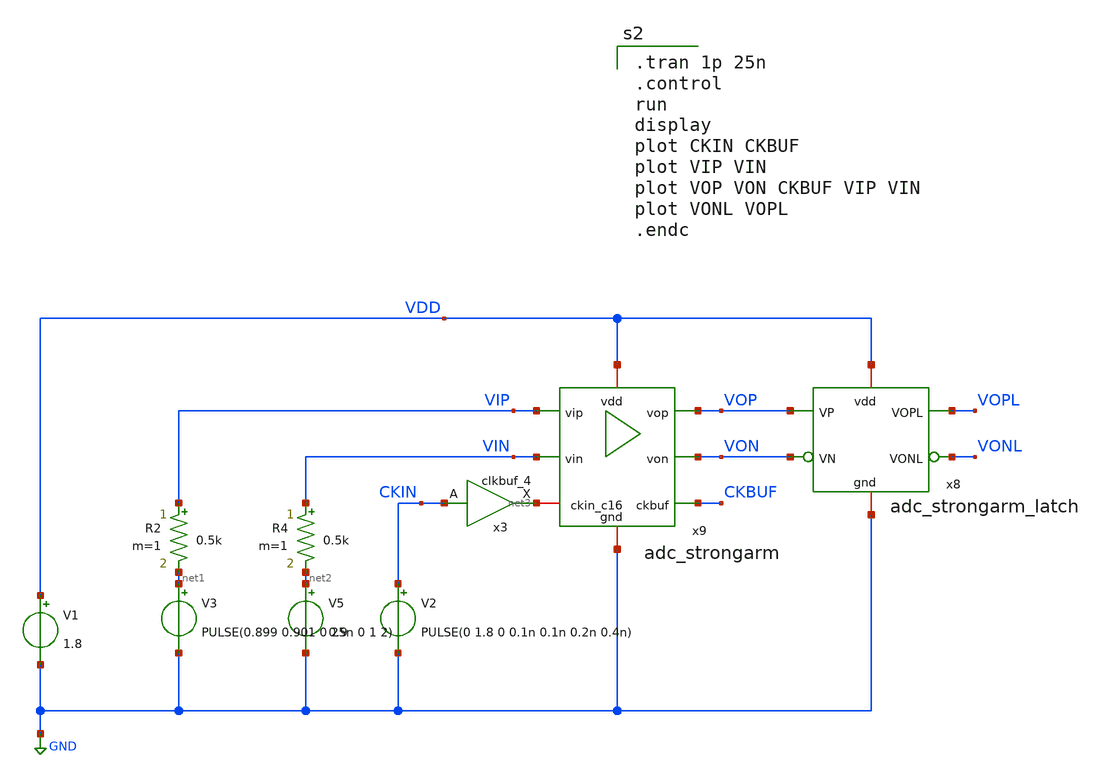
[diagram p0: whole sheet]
** sch_path: xschem/adc_strongarm_tb.sch
**.subckt adc_strongarm_tb
V1 VDD GND 1.8
V2 CKIN GND PULSE(0 1.8 0 0.1n 0.1n 0.2n 0.4n)
V3 net1 GND PULSE(0.899 0.901 0 25n 0 1 2)
x3 CKIN GND GND VDD VDD net3 sky130_fd_sc_hs__clkbuf_4
R2 VIP net1 0.5k m=1
x8 VONL VOPL VDD GND VOP VON adc_strongarm_latch
x9 VDD VOP VON VIP VIN net3 GND CKBUF adc_strongarm
V5 net2 GND 0.9
R4 VIN net2 0.5k m=1
**** begin user architecture code

.tran 1p 25n
.control
run
display
plot CKIN CKBUF
plot VIP VIN
plot VOP VON CKBUF VIP VIN
plot VONL VOPL
.endc


.lib $::SKYWATER_MODELS/sky130.lib.spice tt
.include $::PDKPATH/libs.ref/sky130_fd_sc_hs/spice/sky130_fd_sc_hs.spice

**** end user architecture code
**.ends

* expanding   symbol:  adc_strongarm_latch.sym # of pins=6
** sym_path: xschem/adc_strongarm_latch.sym
** sch_path: xschem/adc_strongarm_latch.sch
.subckt adc_strongarm_latch VONL VOPL vdd gnd VP VN
*.iopin vdd
*.iopin gnd
*.ipin VP
*.ipin VN
*.opin VOPL
*.opin VONL
XM11 VOPL net1 gnd gnd sky130_fd_pr__nfet_01v8 L=0.15 W=5 nf=1 ad='int((nf+1)/2) * W/nf * 0.29' as='int((nf+2)/2) * W/nf * 0.29'
+ pd='2*int((nf+1)/2) * (W/nf + 0.29)' ps='2*int((nf+2)/2) * (W/nf + 0.29)' nrd='0.29 / W' nrs='0.29 / W'
+ sa=0 sb=0 sd=0 mult=1 m=1
XM12 VONL net2 gnd gnd sky130_fd_pr__nfet_01v8 L=0.15 W=5 nf=1 ad='int((nf+1)/2) * W/nf * 0.29' as='int((nf+2)/2) * W/nf * 0.29'
+ pd='2*int((nf+1)/2) * (W/nf + 0.29)' ps='2*int((nf+2)/2) * (W/nf + 0.29)' nrd='0.29 / W' nrs='0.29 / W'
+ sa=0 sb=0 sd=0 mult=1 m=1
x6 VOPL gnd gnd vdd vdd VONL sky130_fd_sc_hd__inv_1
x7 VONL gnd gnd vdd vdd VOPL sky130_fd_sc_hd__inv_1
x1 VP gnd gnd vdd vdd net1 sky130_fd_sc_hd__inv_1
x2 VN gnd gnd vdd vdd net2 sky130_fd_sc_hd__inv_1
.ends


* expanding   symbol:  adc_strongarm.sym # of pins=8
** sym_path: xschem/adc_strongarm.sym
** sch_path: xschem/adc_strongarm.sch
.subckt adc_strongarm vdd vop von vip vin ckin_c16 gnd ckbuf
*.ipin vip
*.ipin vin
*.iopin gnd
*.iopin vdd
*.opin vop
*.opin von
*.iopin ckin_c16
*.opin ckbuf
XM1 net3 vip net1 gnd sky130_fd_pr__nfet_01v8 L=0.15 W=10 nf=1 ad='int((nf+1)/2) * W/nf * 0.29' as='int((nf+2)/2) * W/nf * 0.29'
+ pd='2*int((nf+1)/2) * (W/nf + 0.29)' ps='2*int((nf+2)/2) * (W/nf + 0.29)' nrd='0.29 / W' nrs='0.29 / W'
+ sa=0 sb=0 sd=0 mult=2 m=2
XM2 net2 vin net1 gnd sky130_fd_pr__nfet_01v8 L=0.15 W=10 nf=1 ad='int((nf+1)/2) * W/nf * 0.29' as='int((nf+2)/2) * W/nf * 0.29'
+ pd='2*int((nf+1)/2) * (W/nf + 0.29)' ps='2*int((nf+2)/2) * (W/nf + 0.29)' nrd='0.29 / W' nrs='0.29 / W'
+ sa=0 sb=0 sd=0 mult=2 m=2
XM3 net1 ckbuf gnd gnd sky130_fd_pr__nfet_01v8 L=0.15 W=20 nf=1 ad='int((nf+1)/2) * W/nf * 0.29' as='int((nf+2)/2) * W/nf * 0.29'
+ pd='2*int((nf+1)/2) * (W/nf + 0.29)' ps='2*int((nf+2)/2) * (W/nf + 0.29)' nrd='0.29 / W' nrs='0.29 / W'
+ sa=0 sb=0 sd=0 mult=2 m=2
XM4 vop von net3 gnd sky130_fd_pr__nfet_01v8 L=0.15 W=10 nf=1 ad='int((nf+1)/2) * W/nf * 0.29' as='int((nf+2)/2) * W/nf * 0.29'
+ pd='2*int((nf+1)/2) * (W/nf + 0.29)' ps='2*int((nf+2)/2) * (W/nf + 0.29)' nrd='0.29 / W' nrs='0.29 / W'
+ sa=0 sb=0 sd=0 mult=2 m=2
XM5 von vop net2 gnd sky130_fd_pr__nfet_01v8 L=0.15 W=10 nf=1 ad='int((nf+1)/2) * W/nf * 0.29' as='int((nf+2)/2) * W/nf * 0.29'
+ pd='2*int((nf+1)/2) * (W/nf + 0.29)' ps='2*int((nf+2)/2) * (W/nf + 0.29)' nrd='0.29 / W' nrs='0.29 / W'
+ sa=0 sb=0 sd=0 mult=2 m=2
XM6 von vop vdd vdd sky130_fd_pr__pfet_01v8 L=0.15 W=20 nf=1 ad='int((nf+1)/2) * W/nf * 0.29' as='int((nf+2)/2) * W/nf * 0.29'
+ pd='2*int((nf+1)/2) * (W/nf + 0.29)' ps='2*int((nf+2)/2) * (W/nf + 0.29)' nrd='0.29 / W' nrs='0.29 / W'
+ sa=0 sb=0 sd=0 mult=2 m=2
XM7 vop von vdd vdd sky130_fd_pr__pfet_01v8 L=0.15 W=20 nf=1 ad='int((nf+1)/2) * W/nf * 0.29' as='int((nf+2)/2) * W/nf * 0.29'
+ pd='2*int((nf+1)/2) * (W/nf + 0.29)' ps='2*int((nf+2)/2) * (W/nf + 0.29)' nrd='0.29 / W' nrs='0.29 / W'
+ sa=0 sb=0 sd=0 mult=2 m=2
XM8 vop ckbuf vdd vdd sky130_fd_pr__pfet_01v8 L=0.15 W=10 nf=1 ad='int((nf+1)/2) * W/nf * 0.29' as='int((nf+2)/2) * W/nf * 0.29'
+ pd='2*int((nf+1)/2) * (W/nf + 0.29)' ps='2*int((nf+2)/2) * (W/nf + 0.29)' nrd='0.29 / W' nrs='0.29 / W'
+ sa=0 sb=0 sd=0 mult=2 m=2
XM9 von ckbuf vdd vdd sky130_fd_pr__pfet_01v8 L=0.15 W=10 nf=1 ad='int((nf+1)/2) * W/nf * 0.29' as='int((nf+2)/2) * W/nf * 0.29'
+ pd='2*int((nf+1)/2) * (W/nf + 0.29)' ps='2*int((nf+2)/2) * (W/nf + 0.29)' nrd='0.29 / W' nrs='0.29 / W'
+ sa=0 sb=0 sd=0 mult=2 m=2
x1 ckbuf gnd gnd vdd vdd net4 sky130_fd_sc_hd__inv_4
XM10 net2 net4 net3 gnd sky130_fd_pr__nfet_01v8 L=0.15 W=10 nf=1 ad='int((nf+1)/2) * W/nf * 0.29' as='int((nf+2)/2) * W/nf * 0.29'
+ pd='2*int((nf+1)/2) * (W/nf + 0.29)' ps='2*int((nf+2)/2) * (W/nf + 0.29)' nrd='0.29 / W' nrs='0.29 / W'
+ sa=0 sb=0 sd=0 mult=2 m=2
x2 ckin_c16 gnd gnd vdd vdd ckbuf sky130_fd_sc_hd__clkbuf_16
.ends

.GLOBAL GND
.end
